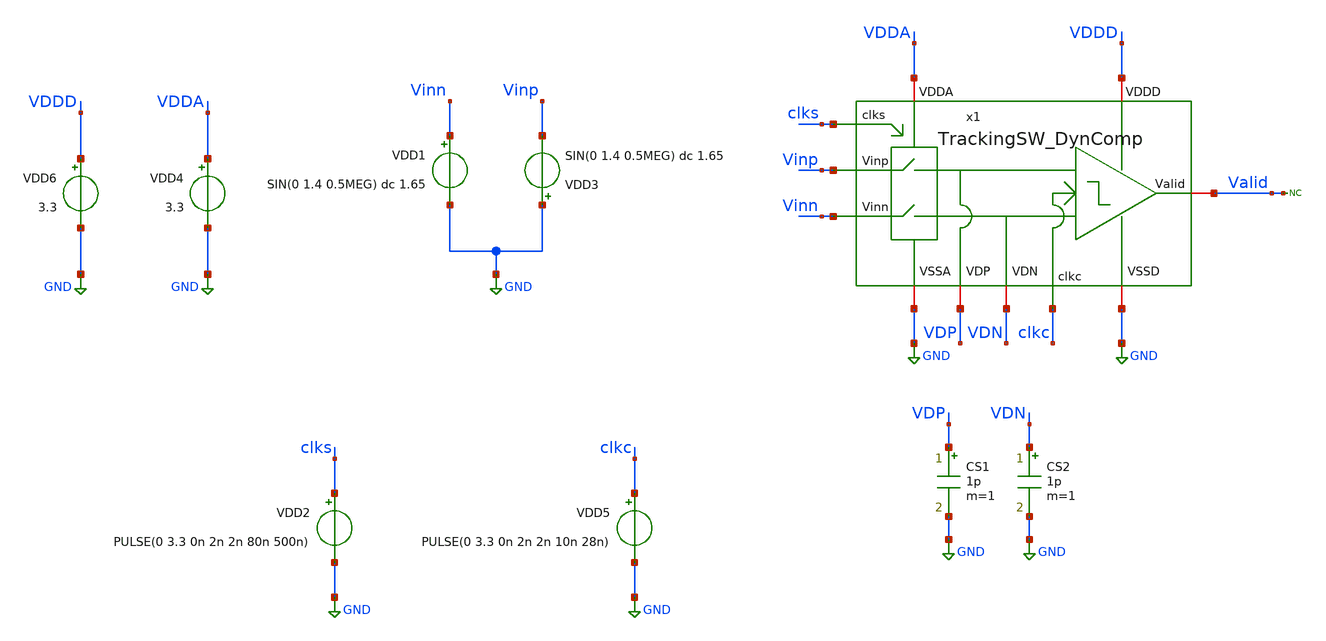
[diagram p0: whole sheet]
** sch_path: SAR_ADC/integration/TrackingSW_DynComp_tb.sch
**.subckt TrackingSW_DynComp_tb
x1 VDDA GND VDDD Valid GND VDP clks VDN clkc Vinp Vinn TrackingSW_DynComp
CS1 VDP GND 1p m=1
CS2 VDN GND 1p m=1
* noconn Valid
VDD2 clks GND PULSE(0 3.3 0n 2n 2n 80n 500n)
VDD4 VDDA GND 3.3
VDD1 Vinn GND SIN(0 1.4 0.5MEG) dc 1.65
VDD3 GND Vinp SIN(0 1.4 0.5MEG) dc 1.65
VDD5 clkc GND PULSE(0 3.3 0n 2n 2n 10n 28n)
VDD6 VDDD GND 3.3
**** begin user architecture code



*Parameters

.options TEMP = 50.0
.lib /home/electrica/Documents/gf180_projects/pdk/gf180mcuC/libs.tech/ngspice/sm141064.ngspice typical
.include /home/electrica/Documents/gf180_projects/pdk/gf180mcuC/libs.tech/ngspice/design.ngspice

*Data to save
.save all


* Simulation
.control
tran 0.1n 5u 0.01n
*setplot dc1
plot V(Vinp)+40 V(Vinn)+36 V(clks)+32 V(VDP)+28 V(VDN)+28 V(.x1.x3.aN)+24 V(.x1.x3.aP)+20
+ V(.x1.x3.dN)+16 V(.x1.x3.dP)+12 V(.x1.x3.Vocp)+8 V(.x1.x3.Vocn)+4 V(Valid)
set filetype = ascii
write TrackingSW_DynComp_tb_tran.raw

reset
unset filetype
op
save all
write TrackingSW_DynComp_tb.raw


.endc
.end


**** end user architecture code
**.ends
.GLOBAL GND
.end
